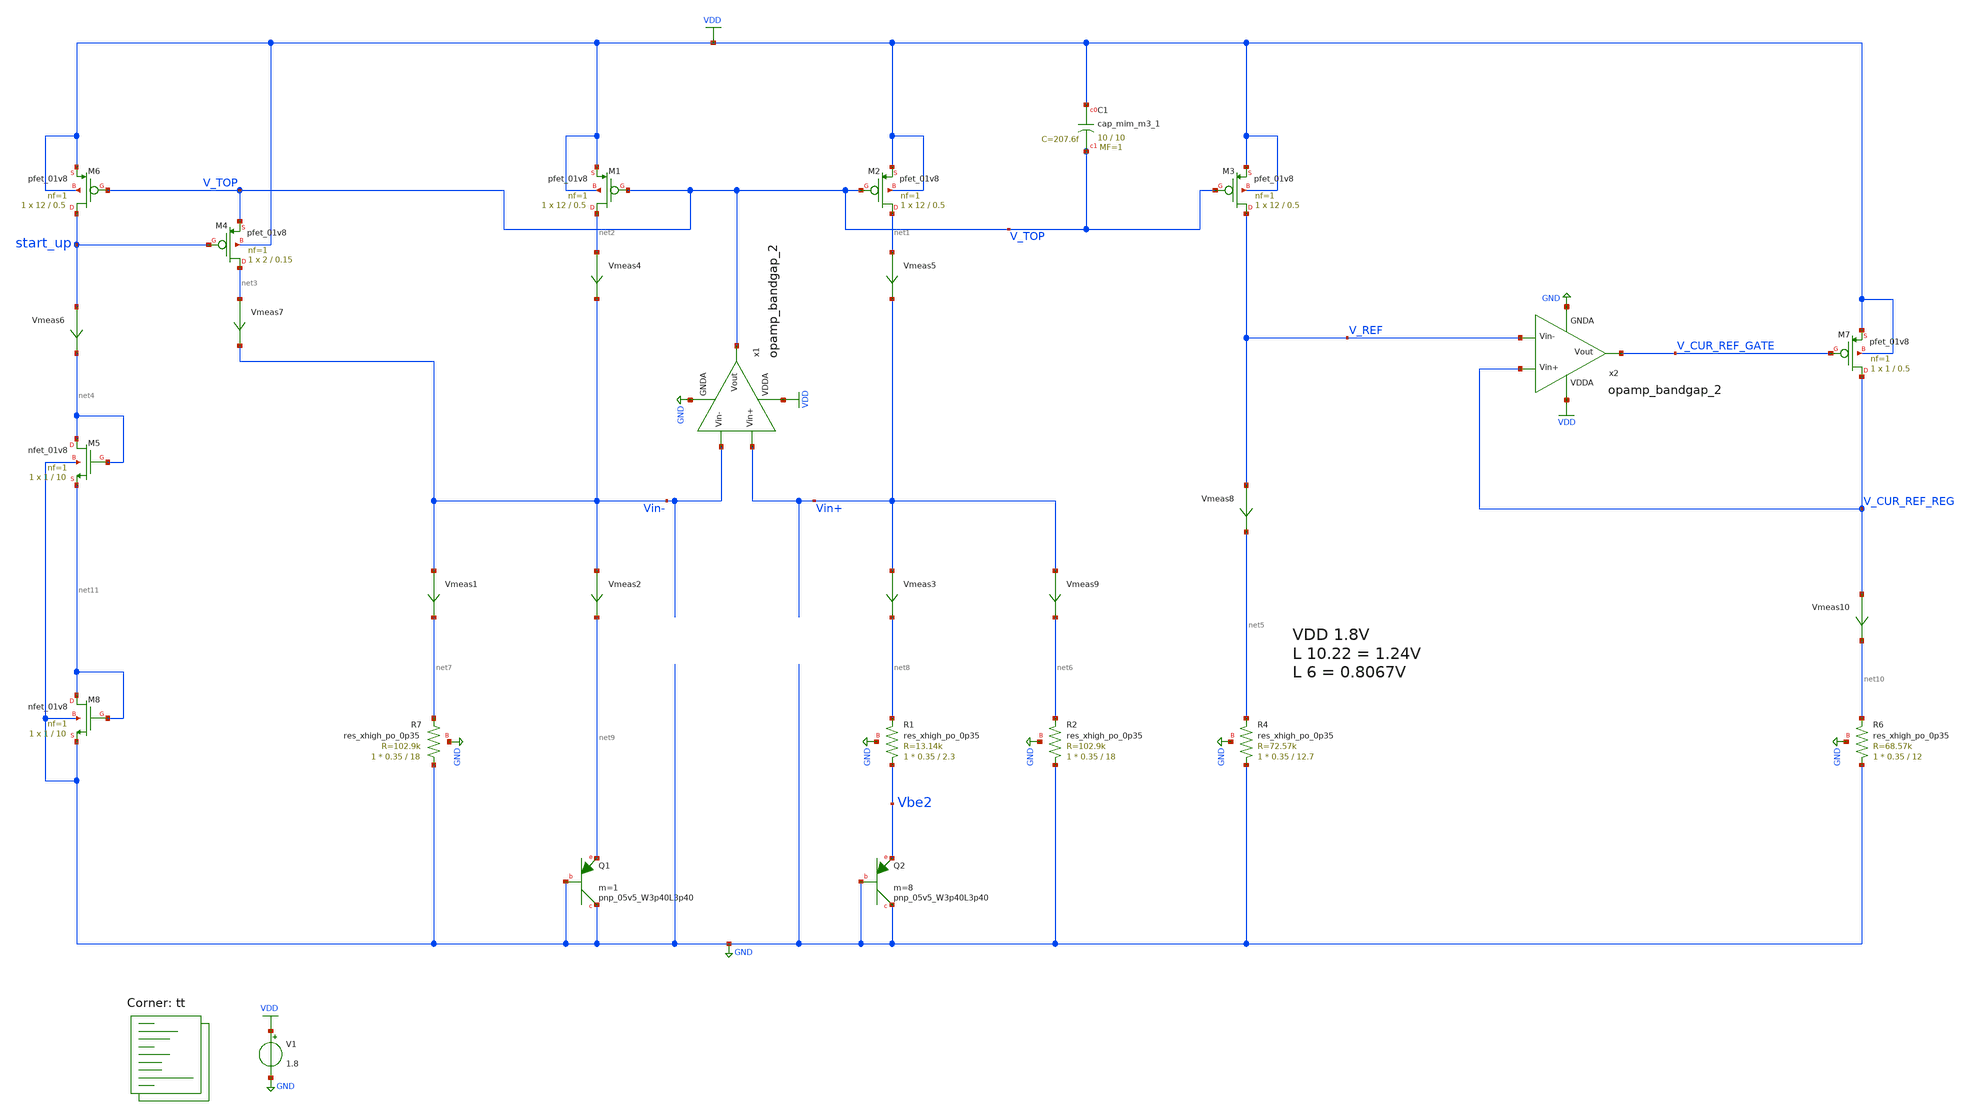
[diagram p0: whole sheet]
** sch_path: projects/bandgapref/xschem_ngspice/new_files/tb_ref_current_gen.sch
**.subckt tb_ref_current_gen
V1 VDD GND 1.8
XQ1 GND GND net9 sky130_fd_pr__pnp_05v5_W3p40L3p40 m=1
XQ2 GND GND Vbe2 sky130_fd_pr__pnp_05v5_W3p40L3p40 m=8
XM1 net2 V_TOP VDD VDD sky130_fd_pr__pfet_01v8 L=0.5 W=12 nf=1 ad='int((nf+1)/2) * W/nf * 0.29' as='int((nf+2)/2) * W/nf * 0.29'
+ pd='2*int((nf+1)/2) * (W/nf + 0.29)' ps='2*int((nf+2)/2) * (W/nf + 0.29)' nrd='0.29 / W' nrs='0.29 / W'
+ sa=0 sb=0 sd=0 mult=1 m=1
XM2 net1 V_TOP VDD VDD sky130_fd_pr__pfet_01v8 L=0.5 W=12 nf=1 ad='int((nf+1)/2) * W/nf * 0.29' as='int((nf+2)/2) * W/nf * 0.29'
+ pd='2*int((nf+1)/2) * (W/nf + 0.29)' ps='2*int((nf+2)/2) * (W/nf + 0.29)' nrd='0.29 / W' nrs='0.29 / W'
+ sa=0 sb=0 sd=0 mult=1 m=1
XM3 V_REF V_TOP VDD VDD sky130_fd_pr__pfet_01v8 L=0.5 W=12 nf=1 ad='int((nf+1)/2) * W/nf * 0.29' as='int((nf+2)/2) * W/nf * 0.29'
+ pd='2*int((nf+1)/2) * (W/nf + 0.29)' ps='2*int((nf+2)/2) * (W/nf + 0.29)' nrd='0.29 / W' nrs='0.29 / W'
+ sa=0 sb=0 sd=0 mult=1 m=1
XR1 Vbe2 net8 GND sky130_fd_pr__res_xhigh_po_0p35 L=2.3 mult=1 m=1
XR2 GND net6 GND sky130_fd_pr__res_xhigh_po_0p35 L=18 mult=1 m=1
XR4 GND net5 GND sky130_fd_pr__res_xhigh_po_0p35 L=12.7 mult=1 m=1
Vmeas4 net2 Vin- 0
.save i(vmeas4)
XM5 net4 net4 net11 GND sky130_fd_pr__nfet_01v8 L=10 W=1 nf=1 ad='int((nf+1)/2) * W/nf * 0.29' as='int((nf+2)/2) * W/nf * 0.29'
+ pd='2*int((nf+1)/2) * (W/nf + 0.29)' ps='2*int((nf+2)/2) * (W/nf + 0.29)' nrd='0.29 / W' nrs='0.29 / W'
+ sa=0 sb=0 sd=0 mult=1 m=1
XM6 start_up V_TOP VDD VDD sky130_fd_pr__pfet_01v8 L=0.5 W=12 nf=1 ad='int((nf+1)/2) * W/nf * 0.29' as='int((nf+2)/2) * W/nf * 0.29'
+ pd='2*int((nf+1)/2) * (W/nf + 0.29)' ps='2*int((nf+2)/2) * (W/nf + 0.29)' nrd='0.29 / W' nrs='0.29 / W'
+ sa=0 sb=0 sd=0 mult=1 m=1
Vmeas5 net1 Vin+ 0
.save i(vmeas5)
XM4 net3 start_up V_TOP VDD sky130_fd_pr__pfet_01v8 L=0.15 W=2 nf=1 ad='int((nf+1)/2) * W/nf * 0.29'
+ as='int((nf+2)/2) * W/nf * 0.29' pd='2*int((nf+1)/2) * (W/nf + 0.29)' ps='2*int((nf+2)/2) * (W/nf + 0.29)'
+ nrd='0.29 / W' nrs='0.29 / W' sa=0 sb=0 sd=0 mult=1 m=1
Vmeas7 net3 Vin- 0
.save i(vmeas7)
XR7 GND net7 GND sky130_fd_pr__res_xhigh_po_0p35 L=18 mult=1 m=1
Vmeas8 V_REF net5 0
.save i(vmeas8)
Vmeas6 start_up net4 0
.save i(vmeas6)
Vmeas1 Vin- net7 0
.save i(vmeas1)
Vmeas2 Vin- net9 0
.save i(vmeas2)
Vmeas3 Vin+ net8 0
.save i(vmeas3)
Vmeas9 Vin+ net6 0
.save i(vmeas9)
XR6 GND net10 GND sky130_fd_pr__res_xhigh_po_0p35 L=12 mult=1 m=1
XM7 V_CUR_REF_REG V_CUR_REF_GATE VDD VDD sky130_fd_pr__pfet_01v8 L=0.5 W=1 nf=1 ad='int((nf+1)/2) * W/nf * 0.29'
+ as='int((nf+2)/2) * W/nf * 0.29' pd='2*int((nf+1)/2) * (W/nf + 0.29)' ps='2*int((nf+2)/2) * (W/nf + 0.29)'
+ nrd='0.29 / W' nrs='0.29 / W' sa=0 sb=0 sd=0 mult=1 m=1
Vmeas10 V_CUR_REF_REG net10 0
.save i(vmeas10)
XM8 net11 net11 GND GND sky130_fd_pr__nfet_01v8 L=10 W=1 nf=1 ad='int((nf+1)/2) * W/nf * 0.29' as='int((nf+2)/2) * W/nf * 0.29'
+ pd='2*int((nf+1)/2) * (W/nf + 0.29)' ps='2*int((nf+2)/2) * (W/nf + 0.29)' nrd='0.29 / W' nrs='0.29 / W'
+ sa=0 sb=0 sd=0 mult=1 m=1
XC1 VDD V_TOP sky130_fd_pr__cap_mim_m3_1 W=10 L=10 MF=1 m=1
x1 VDD V_TOP Vin- Vin+ GND opamp_bandgap_2
x2 VDD V_CUR_REF_GATE V_REF V_CUR_REF_REG GND opamp_bandgap_2
**** begin user architecture code
.lib $::SKYWATER_MODELS/sky130.lib.spice tt



* ngspice commands


.option method=gear
.option wnflag=1
.option savecurrents
* .temp =140

.save @m.xm1.msky130_fd_pr__pfet_01v8[gm] @m.xm1.msky130_fd_pr__pfet_01v8[vth] @m.xm1.msky130_fd_pr__pfet_01v8[vgs] @m.xm1.msky130_fd_pr__pfet_01v8[vds] @m.xm2.msky130_fd_pr__pfet_01v8[gm] @m.xm2.msky130_fd_pr__pfet_01v8[vth] @m.xm2.msky130_fd_pr__pfet_01v8[vgs] @m.xm2.msky130_fd_pr__pfet_01v8[vds] @m.xm3.msky130_fd_pr__pfet_01v8[gm] @m.xm4.msky130_fd_pr__pfet_01v8[gm] @m.xm4.msky130_fd_pr__pfet_01v8[vth] @m.xm5.msky130_fd_pr__nfet_01v8[gm] @m.xm5.msky130_fd_pr__nfet_01v8[vth] @m.xm6.msky130_fd_pr__pfet_01v8[gm] @m.xm6.msky130_fd_pr__pfet_01v8[vth] @m.xm7.msky130_fd_pr__nfet_01v8[gm] @m.xm7.msky130_fd_pr__nfet_01v8[vth] @m.xm8.msky130_fd_pr__nfet_01v8[gm] @m.xm8.msky130_fd_pr__nfet_01v8[vth] @m.xm9.msky130_fd_pr__nfet_01v8[gm] @m.xm9.msky130_fd_pr__nfet_01v8[vth] @m.x1.xm1.msky130_fd_pr__nfet_01v8[gm] @m.x1.xm2.msky130_fd_pr__nfet_01v8[gm] @m.x1.xm3.msky130_fd_pr__nfet_01v8[gm] @m.x1.xm4.msky130_fd_pr__nfet_01v8[gm] @m.x1.xm5.msky130_fd_pr__pfet_01v8[gm] @m.x1.xm6.msky130_fd_pr__nfet_01v8[gm] @m.x1.xm7.msky130_fd_pr__pfet_01v8[gm]

* .ic v(vin-) = 0.8
* .ic v(vin+) = 0.8
* .ic v(v_top) = 1.8

.control

    save all
    * dc temp -40 120 5 V1 1.6 2.0 0.05
    * dc V1 1.7 1.9 0.001 temp -40 120 40
    dc V1 0.0 2.0 0.02 temp -40 120 20
    * dc V1 0 2.0 0.02
    * tran 0.1ns 3us
    remzerovec
    write tb_ref_current_gen.raw
.endc




**** end user architecture code
**.ends

* expanding   symbol:  opamp_bandgap_2.sym # of pins=5
** sym_path: projects/bandgapref/xschem_ngspice/new_files/opamp_bandgap_2.sym
** sch_path: projects/bandgapref/xschem_ngspice/new_files/opamp_bandgap_2.sch
.subckt opamp_bandgap_2 VDDA Vout Vin- Vin+ GNDA
*.ipin Vin+
*.opin Vout
*.ipin Vin-
*.ipin GNDA
*.ipin VDDA
XM1 V_p VDDA GNDA GNDA sky130_fd_pr__nfet_01v8 L=5 W=2.5 nf=1 ad='int((nf+1)/2) * W/nf * 0.29' as='int((nf+2)/2) * W/nf * 0.29'
+ pd='2*int((nf+1)/2) * (W/nf + 0.29)' ps='2*int((nf+2)/2) * (W/nf + 0.29)' nrd='0.29 / W' nrs='0.29 / W'
+ sa=0 sb=0 sd=0 mult=1 m=1
XM2 V_mirror Vin- V_p GNDA sky130_fd_pr__nfet_01v8 L=0.2 W=2.5 nf=1 ad='int((nf+1)/2) * W/nf * 0.29'
+ as='int((nf+2)/2) * W/nf * 0.29' pd='2*int((nf+1)/2) * (W/nf + 0.29)' ps='2*int((nf+2)/2) * (W/nf + 0.29)'
+ nrd='0.29 / W' nrs='0.29 / W' sa=0 sb=0 sd=0 mult=1 m=1
XM3 1st_Vout Vin+ V_p GNDA sky130_fd_pr__nfet_01v8 L=0.2 W=2.5 nf=1 ad='int((nf+1)/2) * W/nf * 0.29'
+ as='int((nf+2)/2) * W/nf * 0.29' pd='2*int((nf+1)/2) * (W/nf + 0.29)' ps='2*int((nf+2)/2) * (W/nf + 0.29)'
+ nrd='0.29 / W' nrs='0.29 / W' sa=0 sb=0 sd=0 mult=1 m=1
XM5 V_mirror V_mirror VDDA VDDA sky130_fd_pr__pfet_01v8 L=0.2 W=6 nf=2 ad='int((nf+1)/2) * W/nf * 0.29'
+ as='int((nf+2)/2) * W/nf * 0.29' pd='2*int((nf+1)/2) * (W/nf + 0.29)' ps='2*int((nf+2)/2) * (W/nf + 0.29)'
+ nrd='0.29 / W' nrs='0.29 / W' sa=0 sb=0 sd=0 mult=1 m=1
XM6 1st_Vout V_mirror VDDA VDDA sky130_fd_pr__pfet_01v8 L=0.2 W=6 nf=2 ad='int((nf+1)/2) * W/nf * 0.29'
+ as='int((nf+2)/2) * W/nf * 0.29' pd='2*int((nf+1)/2) * (W/nf + 0.29)' ps='2*int((nf+2)/2) * (W/nf + 0.29)'
+ nrd='0.29 / W' nrs='0.29 / W' sa=0 sb=0 sd=0 mult=1 m=1
XM4 Vout VDDA GNDA GNDA sky130_fd_pr__nfet_01v8 L=5 W=2.5 nf=1 ad='int((nf+1)/2) * W/nf * 0.29' as='int((nf+2)/2) * W/nf * 0.29'
+ pd='2*int((nf+1)/2) * (W/nf + 0.29)' ps='2*int((nf+2)/2) * (W/nf + 0.29)' nrd='0.29 / W' nrs='0.29 / W'
+ sa=0 sb=0 sd=0 mult=1 m=1
XM7 Vout 1st_Vout VDDA VDDA sky130_fd_pr__pfet_01v8 L=0.2 W=6 nf=2 ad='int((nf+1)/2) * W/nf * 0.29' as='int((nf+2)/2) * W/nf * 0.29'
+ pd='2*int((nf+1)/2) * (W/nf + 0.29)' ps='2*int((nf+2)/2) * (W/nf + 0.29)' nrd='0.29 / W' nrs='0.29 / W'
+ sa=0 sb=0 sd=0 mult=1 m=1
XC1 1st_Vout net1 sky130_fd_pr__cap_mim_m3_1 W=10 L=10 MF=1 m=1
XR1 Vout net1 GNDA sky130_fd_pr__res_xhigh_po_0p35 L=0.5 mult=1 m=1
.ends

.GLOBAL GND
.GLOBAL VDD
.end
